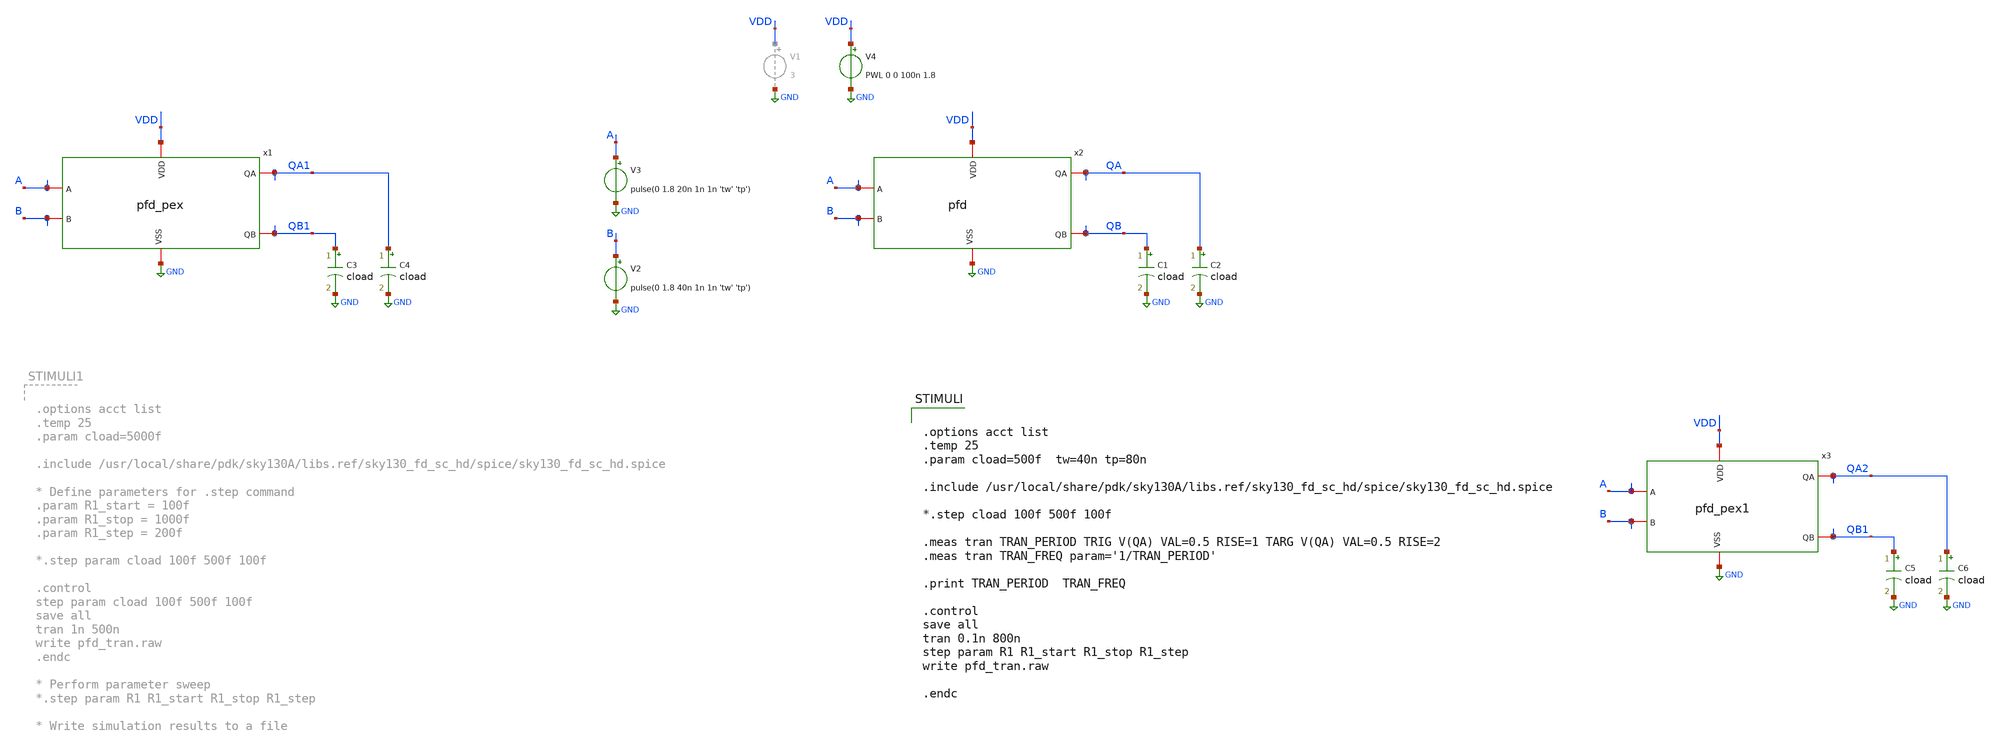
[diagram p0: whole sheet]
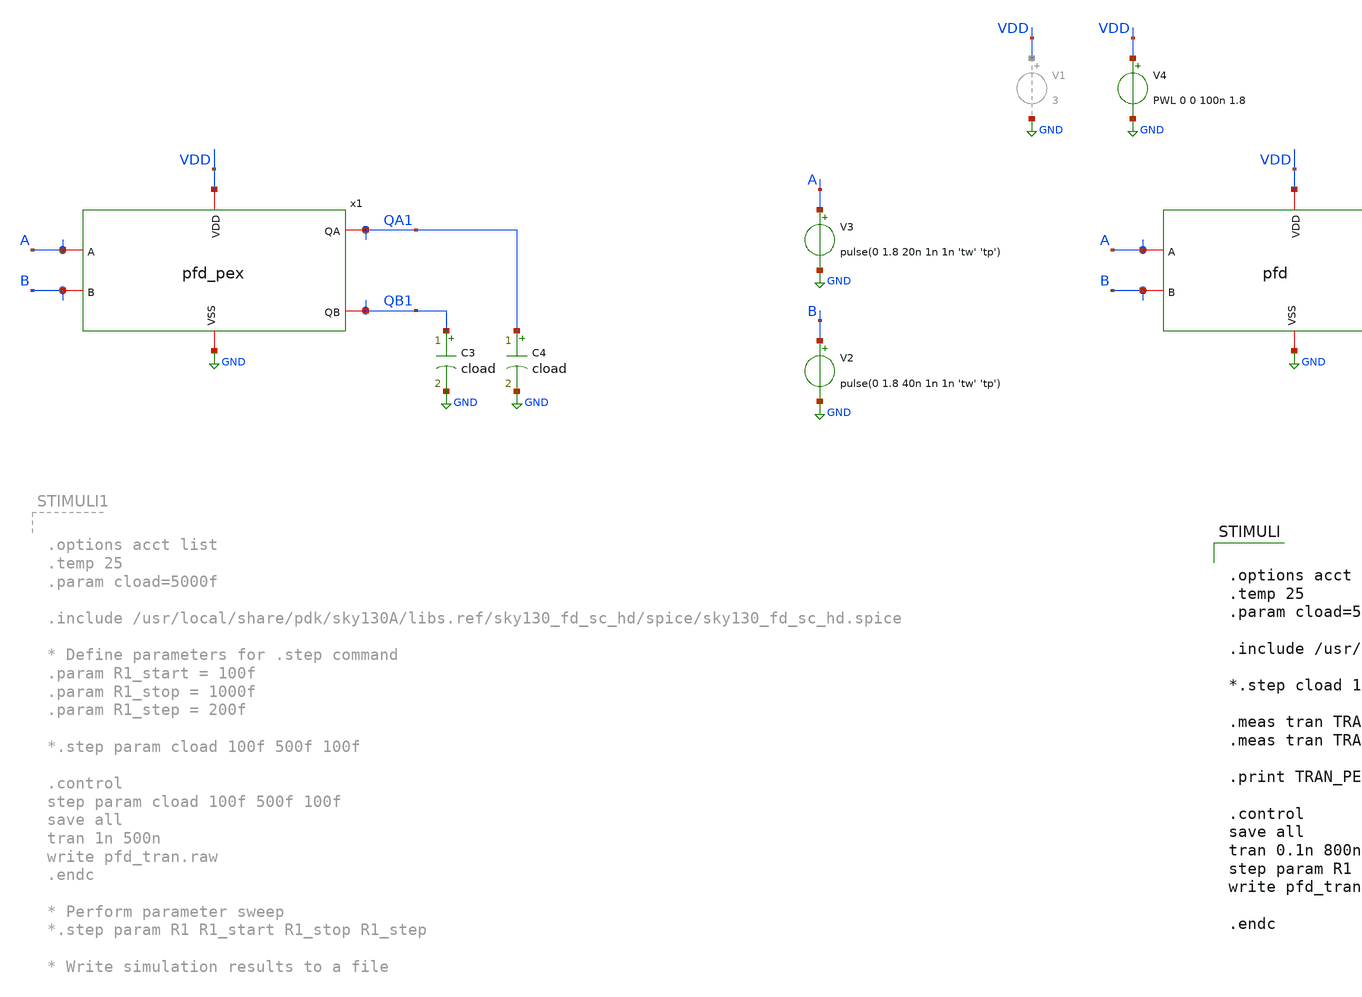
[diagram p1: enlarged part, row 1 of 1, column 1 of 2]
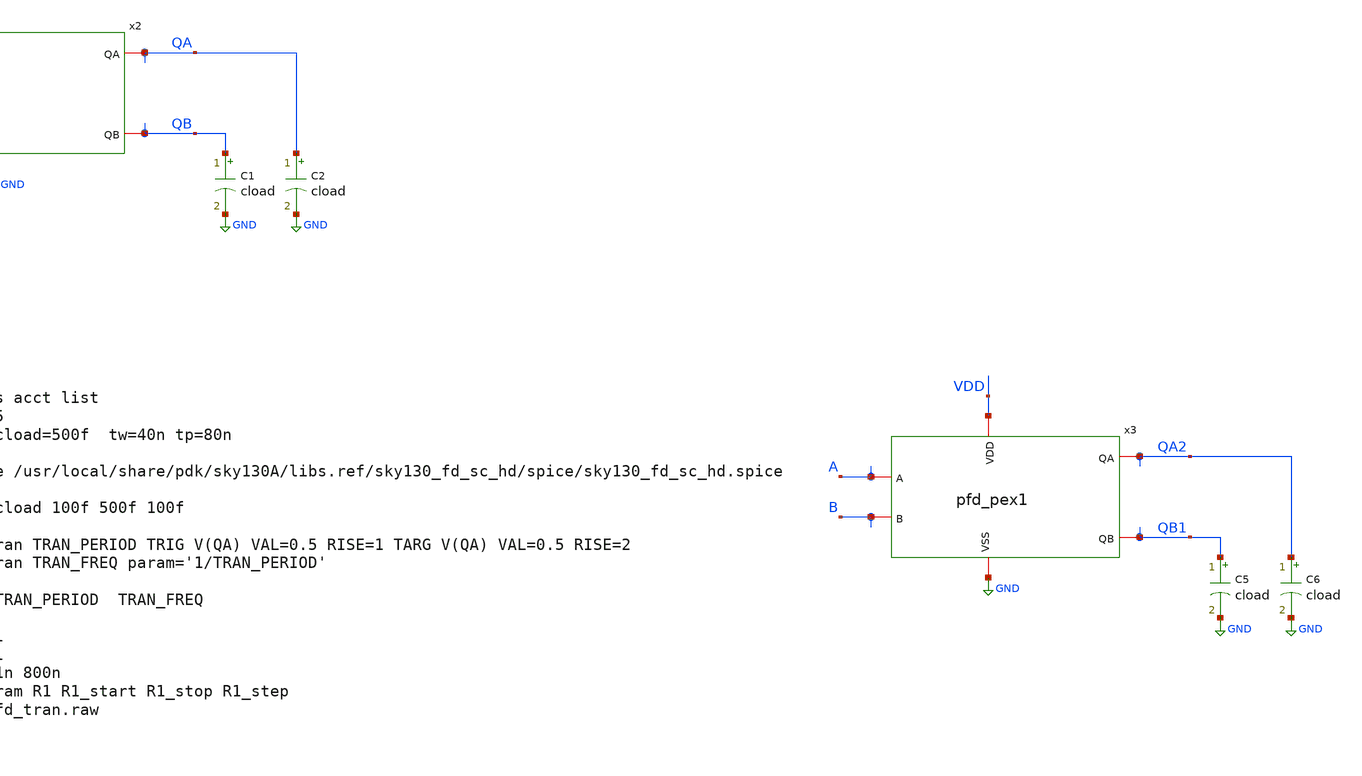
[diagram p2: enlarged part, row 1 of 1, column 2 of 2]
** sch_path: xschem/pfd/pfd_tran1.sch
**.subckt pfd_tran1
V2 B GND pulse(0 1.8 40n 1n 1n 'tw' 'tp')
V3 A GND pulse(0 1.8 20n 1n 1n 'tw' 'tp')
C1 QB GND cload m=1
C2 QA GND cload m=1
V4 VDD GND PWL 0 0 100n 1.8
C3 QB1 GND cload m=1
C4 QA1 GND cload m=1
x1 GND VDD A QA1 QB1 B pfd_pex
x2 GND VDD A QA QB B pfd
C5 QB1 GND cload m=1
C6 QA2 GND cload m=1
x3 GND VDD A QA2 QB1 B pfd_pex1
**** begin user architecture code


.options acct list
.temp 25
.param cload=500f  tw=40n tp=80n

.include /usr/local/share/pdk/sky130A/libs.ref/sky130_fd_sc_hd/spice/sky130_fd_sc_hd.spice

*.step cload 100f 500f 100f

.meas tran TRAN_PERIOD TRIG V(QA) VAL=0.5 RISE=1 TARG V(QA) VAL=0.5 RISE=2
.meas tran TRAN_FREQ param='1/TRAN_PERIOD'

.print TRAN_PERIOD  TRAN_FREQ

.control
save all
tran 0.1n 800n
step param R1 R1_start R1_stop R1_step
write pfd_tran.raw

.endc



** opencircuitdesign pdks install
.lib $::SKYWATER_MODELS/sky130.lib.spice tt


**** end user architecture code
**.ends
.GLOBAL GND
.end
